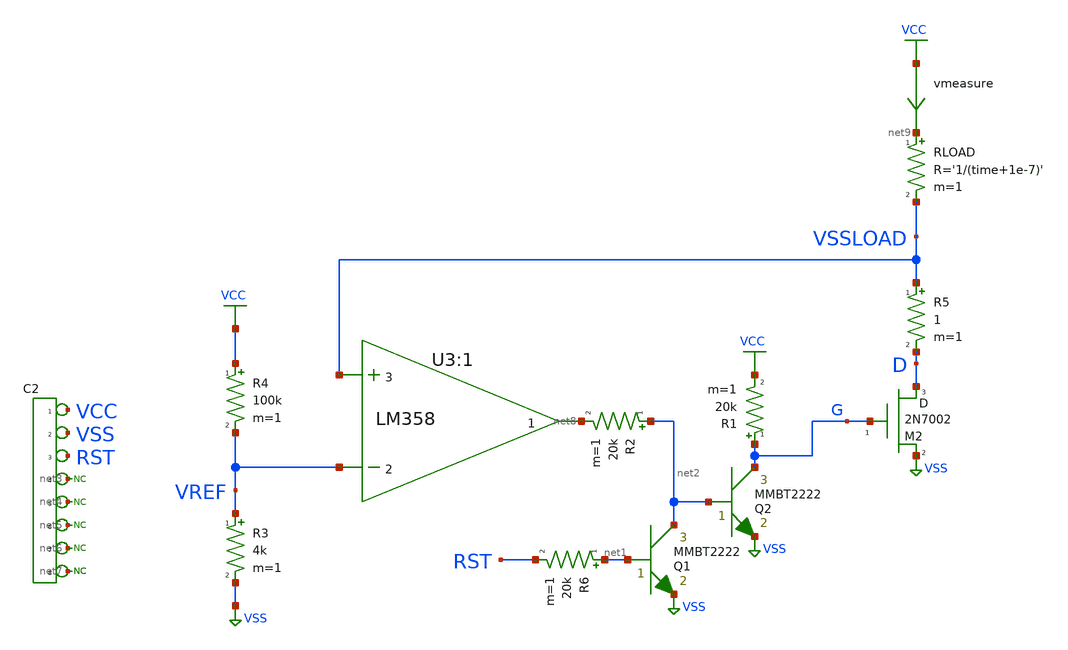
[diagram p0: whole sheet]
** sch_path: xschem_library/pcb/pcb_current_protection.sch
**.subckt pcb_current_protection
*connector(8,1) ?1 VCC ?1 VSS ?1 RST ?1 net3 ?1 net4 ?1 net5 ?1 net6 ?1 net7
* noconn #net7
* noconn #net7
* noconn #net6
XU3:1 VSSLOAD VREF VCC VSS net8 LM358
R3 VREF VSS 4k m=1
R4 VCC VREF 100k m=1
XM2 D G VSS M2N7002 m=1
R5 VSSLOAD D 1 m=1
* noconn #net5
* noconn #net4
* noconn #net3
RLOAD net9 VSSLOAD R='1/(time+1e-7)' m=1
vmeasure VCC net9 0
.save i(vmeasure)
R2 net2 net8 20k m=1
Q1 net2 net1 VSS MMBT2222 area=1 m=1
R6 net1 RST 20k m=1
Q2 G net2 VSS MMBT2222 area=1 m=1
R1 G VCC 20k m=1
**** begin user architecture code


*.option PARHIER=LOCAL RUNLVL=5 post MODMONTE=1 warn maxwarns=400 ingold=1


vvcc vcc 0 dc 5
vvss vss 0 dc 0
vrst rst 0 pwl 0 5 100u 5 101u 0

* .dc RLOAD 10K 1 -0.001
.tran 10u 200m
.save all



.MODEL bd139_2 npn IS=1e-09 BF=222.664 NF=0.85 VAF=36.4079 IKF=0.166126 ISE=5.03418e-09 NE=1.45313
+ BR=1.35467 NR=1.33751 VAR=142.931 IKR=1.66126 ISC=5.02557e-09 NC=3.10227 RB=26.9143 IRB=0.1 RBM=0.1
+ RE=0.000472454 RC=1.04109 XTB=0.727762 XTI=1.04311 EG=1.05 CJE=1e-11 VJE=0.75 MJE=0.33 TF=1e-09 XTF=1 VTF=10
+ ITF=0.01 CJC=1e-11 VJC=0.75 MJC=0.33 XCJC=0.9 FC=0.5 CJS=0 VJS=0.75 MJS=0.5 TR=1e-07 PTF=0 KF=0 AF=1

*SRC=BC817-16;DI_BC817-16;BJTs NPN; Si;  45.0V  0.800A  220MHz   Diodes Inc. BJTs
.MODEL BC817  NPN (IS=4.04n NF=1.00 BF=342 VAF=121  IKF=0.273 ISE=6.86n NE=2.00 BR=4.00 NR=1.00
+  VAR=20.0 IKR=0.675 RE=0.227 RB=0.907 RC=90.7m  XTB=1.5 CJE=107p VJE=1.10 MJE=0.500 CJC=34.7p VJC=0.300
+ MJC=0.300   TF=651p TR=111n EG=1.12 )

.MODEL BD139 NPN ( IS=2.3985E-13 Vceo=80 Icrating=1500m BF=244.9 NF=1.0 BR=78.11 NR=1.007
+ ISE=1.0471E-14 NE=1.2 ISC=1.9314E-11 NC=1.45 VAF=98.5 VAR=7.46 IKF=1.1863 IKR=0.1445 RB=2.14 RBM=0.001 IRB=0.031
+ RE=0.0832 RC=0.01 CJE=2.92702E-10 VJE=0.67412 MJE=0.3300 FC=0.5 CJC=4.8831E-11 VJC=0.5258 MJC=0.3928
+ XCJC=0.5287 XTB=1.1398 EG=1.2105 XTI=3.0)


.MODEL BD140  PNP(IS=1e-09 BF=650.842 NF=0.85 VAF=10 IKF=0.0950125 ISE=1e-08 NE=1.54571 BR=56.177
+ NR=1.5 VAR=2.11267 IKR=0.950125 ISC=1e-08 NC=3.58527 RB=41.7566 IRB=0.1 RBM=0.108893 RE=0.000347052
+ RC=1.32566 XTB=19.5239 XTI=1 EG=1.05 CJE=1e-11 VJE=0.75 MJE=0.33 TF=1e-09 XTF=1 VTF=10 ITF=0.01 CJC=1e-11
+ VJC=0.75 MJC=0.33 XCJC=0.9 FC=0.5 CJS=0 VJS=0.75 MJS=0.5 TR=1e-07 PTF=0 KF=0 AF=10  VCEO=80 ICRATING=1A )


.MODEL Q2N2222A NPN IS =3.0611E-14 NF =1.00124 BF =220 IKF=0.52                VAF=104 ISE=7.5E-15
+ NE =1.41 NR =1.005 BR =4 IKR=0.24                VAR=28 ISC=1.06525E-11 NC =1.3728 RB =0.13 RE =0.22
+                RC =0.12 CJC=9.12E-12 MJC=0.3508 VJC=0.4089                CJE=27.01E-12 TF =0.325E-9 TR =100E-9
+               vce_max=45 vbe_max=6

.MODEL Q2N2222 NPN (  IS = 3.97589E-14 BF = 195.3412 NF = 1.0040078 VAF = 53.081 IKF = 0.976 ISE =
+ 1.60241E-14  NE = 1.4791931 BR = 1.1107942 NR = 0.9928261 VAR = 11.3571702 IKR = 2.4993953 ISC = 1.88505E-12
+  NC = 1.1838278 RB = 56.5826472 IRB = 1.50459E-4 RBM = 5.2592283 RE = 0.0402974 RC = 0.4208  CJE =
+ 2.56E-11 VJE = 0.682256 MJE = 0.3358856 TF = 3.3E-10 XTF = 6 VTF = 0.574  ITF = 0.32 PTF = 25.832 CJC =
+ 1.40625E-11 VJC = 0.5417393 MJC = 0.4547893 XCJC = 1  TR = 3.2E-7 CJS = 0 VJS = .75 MJS = 0 XTB = 1.6486 EG =
+ 1.11  XTI = 5.8315 KF = 0 AF = 1 FC = 0.83               vce_max=45 vbe_max=6 )


* 2n2222 p complementary
.MODEL Q2N2907P PNP(IS=650.6E-18 ISE=54.81E-15 ISC=0 XTI=3  BF=231.7 BR=3.563 IKF=1.079 IKR=0
+ XTB=1.5  VAF=115.7 VAR=35 VJE=0.65 VJC=0.65  RE=0.15 RC=0.715 RB=10  CJE=19.82E-12 CJC=14.76E-12 XCJC=0.75
+ FC=0.5  NF=1 NR=1 NE=1.829 NC=2 MJE=0.3357 MJC=0.5383  TF=603.7E-12 TR=111.3E-9 ITF=0.65 VTF=5 XTF=1.7
+  EG=1.11 KF=1E-9 AF=1  VCEO=45 ICRATING=100M                vce_max=45 vbe_max=6 )

.MODEL Q2N2907S PNP(IS=2.32E-13 ISE=6.69E-16 ISC=1.65E-13 XTI=3.00  BF=3.08E2 BR=2.18E1 IKF=8.42E-1
+ IKR=1.00 XTB=1.5  VAF=1.41E2 VAR=1.35E1 VJE=3.49E-1 VJC=3.00E-1  RE=1.00E-2 RC=8.46E-1 RB=4.02E1 RBM=1.00E-2
+ IRB=1.25E-2  CJE=2.66E-11 CJC=1.93E-11 XCJC=1.00 FC=5.00E-1  NF=1.04 NR=1.12 NE=1.09 NC=1.13 MJE=4.60E-1
+ MJC=4.65E-1  TF=4.95E-10 TR=0 PTF=0 ITF=3.36E-1 VTF=6.54 XTF=1.87E1  EG=1.11 KF=1E-9 AF=1  VCEO=40
+ ICRATING=500M                vce_max=45 vbe_max=6 )





* PINOUT ORDER +IN -IN +V -V OUT
* PINOUT ORDER  1   2   3  4  5
.SUBCKT LM358 1 2 3 4 5
R44 4 6 4E4
I1 4 7 0.5E-6
Q1 4 8 9 QPI
Q2 4 2 10 QPA
Q3 9 9 11 QPI
Q4 10 10 11 QPI
Q5 12 13 4 QNQ
Q6 13 13 4 QNQ
Q7 4 12 14 QPQ
Q8 3 14 6 QNQ
Q9 15 6 4 QNQ
Q10 3 15 16 QNQ
Q11 3 16 17 QNQ
R67 17 16 4E4
R68 5 17 18
Q12 4 15 5 QPQ
Q13 15 17 5 QNQ
I2 18 3 120E-9
I3 19 3 60E-9
I4 20 3 1E-6
Q14 11 18 3 QPQ
Q15 14 19 3 QPQ
Q16 5 7 4 QNQ
Q17 15 20 3 QPQ
C15 21 22 4.8E-12
R69 12 21 3
R70 12 15 3E9
E2 23 8 3 0 -10E-6
V51 23 1 1.56E-3
I6 3 4 5E-6
R71 4 3 4.5E5
Q18 12 9 11 QPQ
Q19 13 10 11 QPQ
C17 12 13 8E-12
C18 6 15 1E-12
C21 3 24 100E-15
R78 11 24 3E5
C22 1 2 0.23E-12
C23 2 0 0.79E-12
C24 1 0 0.79E-12
E3 22 0 15 0 2
C25 5 0 50E-15
Q20 25 25 0 QNQ
G1 3 4 VT 0 3E-4
I7 0 25 1E-3
V53 25 26 0.25
R79 0 26 1E6
E4 VT 0 27 26 1
R80 0 VT 1E6
V54 27 0 0.55
R81 0 27 1E6
.MODEL QPQ PNP IKF=3E-3 RC=300 KF=4.8E-17 BR=1
.MODEL QPA PNP IKF=3E-3 RC=380 IS=1.01E-16 VAF=245 RE=5 RB=1700 BF=300 KF=4.8E-17 BR=1
.MODEL QPI PNP IKF=3E-3 RC=380 IS=1.01E-16 VAF=290 RE=5 RB=1700 BF=306 KF=4.8E-17 BR=1
.MODEL QNQ NPN IKF=5E-3 RC=25  KF=4.8E-17 BR=1
.ENDS
* END SPICE MODEL LM358

.SUBCKT irlml6402 1 2 3
* Node 1 -> Drain
* Node 2 -> Gate
* Node 3 -> Source
M1 9 7 8 8 MM L=100u W=100u
.MODEL MM PMOS LEVEL=1 IS=1e-32 VTO=-1 LAMBDA=0.0111358 KP=12.788 CGSO=5.36099e-06 CGDO=5.54234e-08
RS 8 3 0.0246704
D1 1 3 MD
.MODEL MD D IS=2.03395e-08 RS=0.0432758 N=1.5 BV=20 IBV=0.00025 EG=1 XTI=4 TT=1e-07 CJO=1.11974e-10
+ VJ=0.5 M=0.3 FC=0.5
RDS 3 1 5e+07
RD 9 1 0.0001
RG 2 7 29.2227
D2 5 4 MD1
* Default values used in MD1:
*   RS=0 EG=1.11 XTI=3.0 TT=0
*   BV=infinite IBV=1mA
.MODEL MD1 D IS=1e-32 N=50 CJO=1.68841e-10 VJ=1.50027 M=0.3 FC=1e-08
D3 5 0 MD2
* Default values used in MD2:
*   EG=1.11 XTI=3.0 TT=0 CJO=0
*   BV=infinite IBV=1mA
.MODEL MD2 D IS=1e-10 N=0.4 RS=3e-06
RL 5 10 1
FI2 7 9 VFI2 -1
VFI2 4 0 0
EV16 10 0 9 7 1
CAP 11 10 9.68769e-10
FI1 7 9 VFI1 -1
VFI1 11 6 0
RCAP 6 10 1
D4 6 0 MD3
* Default values used in MD3:
*   EG=1.11 XTI=3.0 TT=0 CJO=0
*   RS=0 BV=infinite IBV=1mA
.MODEL MD3 D IS=1e-10 N=0.4
.ENDS irlml6402

.SUBCKT irf5305s 1 2 3
* Node 1 -> Drain
* Node 2 -> Gate
* Node 3 -> Source
M1 9 7 8 8 MM L=100u W=100u
* Default values used in MM:
* The voltage-dependent capacitances are
* not included. Other default values are:
*   RS=0 RD=0 LD=0 CBD=0 CBS=0 CGBO=0
.MODEL MM PMOS LEVEL=1 IS=1e-32 VTO=-3.45761 LAMBDA=0 KP=10.066 CGSO=1.03141e-05 CGDO=1e-11
RS 8 3 0.0262305
D1 1 3 MD
.MODEL MD D IS=8.90854e-09 RS=0.00921723 N=1.5 BV=55 IBV=0.00025 EG=1.2 XTI=3.13635 TT=1e-07
+ CJO=1.30546e-09 VJ=0.663932 M=0.419045 FC=0.5
RDS 3 1 2.2e+06
RD 9 1 0.0001
RG 2 7 11.0979
D2 5 4 MD1
* Default values used in MD1:
*   RS=0 EG=1.11 XTI=3.0 TT=0
*   BV=infinite IBV=1mA
.MODEL MD1 D IS=1e-32 N=50 CJO=1.63729e-09 VJ=0.791199 M=0.552278 FC=1e-08
D3 5 0 MD2
* Default values used in MD2:
*   EG=1.11 XTI=3.0 TT=0 CJO=0
*   BV=infinite IBV=1mA
.MODEL MD2 D IS=1e-10 N=0.400245 RS=3e-06
RL 5 10 1
FI2 7 9 VFI2 -1
VFI2 4 0 0
EV16 10 0 9 7 1
CAP 11 10 1.89722e-09
FI1 7 9 VFI1 -1
VFI1 11 6 0
RCAP 6 10 1
D4 6 0 MD3
* Default values used in MD3:
*   EG=1.11 XTI=3.0 TT=0 CJO=0
*   RS=0 BV=infinite IBV=1mA
.MODEL MD3 D IS=1e-10 N=0.400245
.ENDS






*MM3725 MCE 5/13/95
*Si    1W  40V 500mA 307MHz pkg:TO-39 3,2,1
.MODEL QMM3725 NPN (IS=50.7F NF=1 BF=162 VAF=113 IKF=.45 ISE=38.2P NE=2  BR=4 NR=1 VAR=24 IKR=.675
+ RE=.263 RB=1.05 RC=.105 XTB=1.5  CJE=62.2P VJE=1.1 MJE=.5 CJC=14.6P VJC=.3 MJC=.3 TF=518P TR=45.9N)

*MPS651 MCE 5/12/95
*Si 625mW  60V    2A 110MHz pkg:TO-92 1,2,3
.MODEL QMPS651 NPN (IS=72.1F NF=1 BF=260 VAF=139 IKF=2.5 ISE=67.1P NE=2  BR=4 NR=1 VAR=20 IKR=3.75
+ RE=28.2M RB=.113 RC=11.3M XTB=1.5  CJE=212P VJE=1.1 MJE=.5 CJC=68.6P VJC=.3 MJC=.3 TF=1.44N TR=1U)

*FCX649 ZETEX Spice model   Last revision  17/7/90   Medium Power
*ZTX Si  1.5W  25V    2A 240MHz pkg:SOT-89 2,1,3
.MODEL QFCX649 NPN(IS=3E-13 BF=225 VAF=80 IKF=2.8 ISE=1.1E-13 NE=1.37   BR=110 NR=0.972 VAR=28
+ IKR=0.8 ISC=6.5E-13 NC=1.372 RB=0.3 RE=0.063   RC=0.07 CJE=3.25E-10 TF=1E-9 CJC=7E-11 TR=1E-8 )

*MPSW01A MCE 5/12/95
*Si    1W  40V    1A 210MHz pkg:TO-92 1,2,3
.MODEL QMPSW01A NPN (IS=18.1F NF=1 BF=273 VAF=113 IKF=.6 ISE=15.7P NE=2  BR=4 NR=1 VAR=20 IKR=.9
+ RE=96.5M RB=.386 RC=38.6M XTB=1.5  CJE=78.7P VJE=1.1 MJE=.5 CJC=17.3P VJC=.3 MJC=.3 TF=757P TR=526N)

*BC546 ZETEX Spice model     Last revision  4/90   General Purpose
*ZTX Si 500mW  65V 200mA 300MHz pkg:TO-92 1,2,3
.MODEL BC546 NPN(IS=1.8E-14 BF=400 NF=0.9955 VAF=80 IKF=0.14 ISE=5E-14   NE=1.46 BR=35.5 NR=1.005
+ VAR=12.5 IKR=0.03 ISC=1.72E-13 NC=1.27 RB=0.56   RE=0.6 RC=0.25 CJE=1.3E-11 TF=6.4E-10 CJC=4E-12 VJC=0.54
+ TR=5.072E-8       vce_max=65 vbe_max=6 )

.MODEL BC857 PNP(        AF= 1.00E+00    BF= 1.96E+02    BR= 3.38E+00   CJC= 9.80E-12       CJE=
+ 1.56E-11   CJS= 0.00E+00    EG= 1.11E+00    FC= 8.28E-01       IKF= 8.35E-01   IKR= 1.60E-02   IRB= 1.31E-06
+    IS= 1.32E-14       ISC= 7.71E-14   ISE= 8.44E-13   ITF= 2.14E-01    KF= 0.00E+00       MJC= 3.49E-01
+   MJE= 4.18E-01   MJS= 3.30E-01    NC= 1.19E+00        NE= 1.83E+00    NF= 1.00E+00    NR= 1.00E+00   PTF=
+ 0.00E+00        RB= 1.00E-02   RBM= 1.00E-02    RC= 1.52E+00    RE= 3.00E-02        TF= 6.05E-10    TR=
+ 0.00E+00   VAF= 5.90E+01   VAR= 1.74E+01       VJC= 3.00E-01   VJE= 8.00E-01   VJS= 7.50E-01   VTF= 4.39E+00
+      XCJC= 1.00E+00   XTB= 0.00E+00   XTF= 5.81E+00   XTI= 3.00E+00)

.MODEL BC556 PNP(       IS=2.059E-14      NF=1.003      ISE=2.971E-15      NE=1.316      BF=227.3
+      IKF=0.08719      VAF=37.2      NR=1.007      ISC=1.339E-14      NC=1.15      BR=7.69      IKR=0.07646
+      VAR=11.42      RB=1      IRB=1E-06      RBM=1      RE=0.688      RC=0.6437      XTB=0      EG=1.11      XTI=3
+      CJE=1.4E-11      VJE=0.5912      MJE=0.3572      TF=7.046E-10      XTF=4.217      VTF=5.367      ITF=0.1947
+      PTF=0      CJC=1.113E-11      VJC=0.1      MJC=0.3414      XCJC=0.6288      TR=1E-32      CJS=0
+      VJS=0.75      MJS=0.333      FC=0.7947      vce_max=65 vbe_max=6 )
*

* NXP Semiconductors
*
* Medium power NPN transistor
* IC   = 1 A
* VCEO = 20 V
* hFE  = 85 - 375 @ 2V/500mA
*
*
*
*
* Package pinning does not match Spice model pinning.
* Package: SOT 223
*
* Package Pin 1: Base
* Package Pin 2: Collector
* Package Pin 3: Emitter
* Package Pin 4: Collector
*
* Extraction date (week/year): 13/2008
* Simulator: Spice 3
*
**********************************************************
*#
.SUBCKT BCP68 1 2 3
*
Q1 1 2 3 BCP68
D1 2 1 DIODE
*
*The diode does not reflect a
*physical device but improves
*only modeling in the reverse
*mode of operation.
*
.MODEL BCP68 NPN   IS = 2.312E-013   NF = 0.988   ISE = 8.851E-014   NE = 2.191   BF = 273   IKF =
+ 5.5   VAF = 50   NR = 0.9885   ISC = 6.808E-014   NC = 3   BR = 155.6   IKR = 4   VAR = 17   RB = 15
+   IRB = 2E-006   RBM = 0.65   RE = 0.073   RC = 0.073   XTB = 0   EG = 1.11   XTI = 3   CJE = 2.678E-010
+   VJE = 0.732   MJE = 0.3484   TF = 5.8E-010   XTF = 1.5   VTF = 2.5   ITF = 1   PTF = 0   CJC =
+ 3.406E-011   VJC = 2   MJC = 0.3142   XCJC = 1   TR = 6.5E-009   CJS = 0   VJS = 0.75   MJS = 0.333   FC =
+ 0.95
.MODEL DIODE D   IS = 2.702E-015   N = 1.2   BV = 1000   IBV = 0.001   RS = 0.1   CJO = 0   VJ = 1
+   M = 0.5   FC = 0   TT = 0   EG = 1.11   XTI = 3
.ENDS

.SUBCKT   D1N5765       2   99
*                      |    |
*                      |    |
*                      |    CATHODE
*                      ANODE
I1  99  4   7.0
D1  2   99   DLOW
D2  2   4   DHIGH
R1  4   99  .1   TC=-6.27E-3,-2.33E-7
*
.MODEL DLOW     D       (          IS = 1.0E-15          RS = 100           N = 2.15          TT =
+ 10.0E-09         CJO = 8.285237E-11          VJ = 1.2076937           M = 0.4053107          EG = 1.664
+         XTI = 10.78          KF = 0          AF = 1          FC = 0.4340008          BV = 5.0         IBV =
+ 1E-4  )
.MODEL DHIGH    D       (          IS = 9.0E-15          RS = 0.30           N = 1.2          TT = 0
+         CJO = 0          VJ = 1           M = .5          EG = 0.1         XTI = -3.84          KF = 0
+          AF = 1          FC = .5          BV = 9.9999E+13         IBV = .001  )
.ENDS

.model D1N4007 D(IS=7.02767n RS=0.0341512 N=1.80803 EG=1.05743 XTI=5 BV=1000 IBV=5e-08 CJO=1e-11
+ VJ=0.7 M=0.5 FC=0.5 TT=1e-07 )

.MODEL D1N4148 D   IS = 4.352E-9   N = 1.906   BV = 110   IBV = 0.0001   RS = 0.6458   CJO =
+ 7.048E-13   VJ = 0.869   M = 0.03   FC = 0.5   TT = 3.48E-9

.MODEL D1n5400 d IS=2.61339e-12 RS=0.0110501 N=1.20576 EG=0.6 XTI=3.1271 BV=50 IBV=1e-05 CJO=1e-11
+ VJ=0.7 M=0.5 FC=0.5 TT=1e-09 KF=0 AF=1
* Model generated on October 12, 2003
* Model format: PSpice


*SYM=POWMOSP
.SUBCKT DMP2035U   10 20 30
*     TERMINALS:  D  G  S
M1   1  2  3  3  PMOS L=0.6U W=0.9
RD  10  1  15m
RS  30  3  4m
RG  20  2  9.45
CGS  2  3  1.42n
EGD 12  30  2  1  1
VFB 14  30  0
FFB  2  1  VFB  1
CGD 13 14  598p
R1  13  30  1.00
D1  13 12  DLIM
DDG 14 15  DCGD
R2  12 15  1.00
D2  30  15  DLIM
DSD 10  3  DSUB
.MODEL PMOS PMOS LEVEL=3 U0=300 VMAX=40k  ETA=0.1m VTO=-1.02 TOX=16.8n NSUB=2e17
.MODEL DCGD D CJO=598p VJ=0.150 M=0.340
.MODEL DSUB D IS=36.1n N=1.50 RS=21.8m BV=20  CJO=40p VJ=0.500 M=0.450
.MODEL DLIM D IS=100U
.ENDS


*March 14, 2005
*Doc. ID: 77621, S-50395, Rev. A
.SUBCKT Si2306BDS 4 1 2
M1  3 1 2 2 NMOS W=573319u L=0.50u
M2  2 1 2 4 PMOS W=573319u L=0.35u
R1  4 3     RTEMP 15E-3
CGS 1 2     110E-12
DBD 2 4     DBD
****************************************************************
.MODEL  NMOS        NMOS ( LEVEL  = 3           TOX    = 5E-8  RS     = 19.5E-3         RD     = 0
+           NSUB   = 1.7E17     kp     = 3.3E-5          UO     = 650               VMAX   = 0               XJ
+     = 5E-7        KAPPA  = 5E-1  ETA    = 1E-4            TPG    = 1    IS     = 0               LD     =
+ 0                               CGSO   = 0               CGDO   = 0           CGBO   = 0   TLEV   = 1
+               BEX    = -1.5        TCV    = 3.9E-3  NFS    = 0.8E12          DELTA  = 0.1)
****************************************************************
.MODEL  PMOS        PMOS ( LEVEL  = 3           TOX    = 5E-8 NSUB    = 2E16            TPG    = -1)
****************************************************************
.MODEL DBD D (CJO=95E-12 VJ=0.38 M=0.20  FC=0.1 IS=1E-12 TT=9.3E-8 N=1 BV=30.2)
****************************************************************
.MODEL RTEMP R (TC1=7E-3 TC2=5.5E-6)
****************************************************************
.ENDS


* Fairchild model
* 2N7002 ELECTRICAL MODEL (SOT-23 Single N-Ch DMOS)
* -----------------------
.SUBCKT  M2N7002  20  10  30
Rg     10    1    1
M1      2    1    3    3    DMOS    L=1u   W=1u
.MODEL DMOS NMOS (VTO='2.1*(-0.0016*TEMPER+1.04)'  KP=0.35  THETA=0.086 VMAX=2.2E5  LEVEL=3)
Cgs     1    3    60p
Rd     20    4    0.3 TC=0.0075
Dds     3    4    DDS
.MODEL     DDS    D(BV='60*(0.00072*TEMPER+0.982)'   M=0.36  CJO=23p   VJ=0.8)
Dbody   3   20    DBODY
.MODEL   DBODY    D(IS=1.4E-13   N=1   RS=40m   TT=100n)
Ra      4    2    0.4 TC=0.0075
Rs      3    5    10m
Ls      5    30   .5n
M2      1    8    6    6   INTER
E2      8    6    4    1   2
.MODEL   INTER    NMOS(VTO=0  KP=10   LEVEL=1)
Cgdmax  7    4    85p
Rcgd    7    4    10meg
Dgd     6    4    DGD
Rdgd    4    6    10meg
.MODEL     DGD    D(M=0.53   CJO=85p   VJ=0.12)
M3      7    9    1    1   INTER
E3      9    1    4    1   -2
.ENDS M2N7002

*SRC=1N4732A;DI_1N4732A;Diodes;Zener <=10V; 4.70V  1.00W   Diodes Inc.  Zener
*SYM=HZEN
.SUBCKT D1N4732A  1   2
*    Terminals    A   K
D1 1 2 DF
DZ 3 1 DR
VZ 2 3 2.99
.MODEL DF D ( IS=87.7p RS=0.620 N=1.10  CJO=214p VJ=0.750 M=0.330 TT=50.1n )
.MODEL DR D ( IS=17.5f RS=0.333 N=2.28 )
.ENDS

* Technology:        DISCRETE DEVICE
* Device:            Zener Diode BZX 55C 5V1
* Type:              Typical (nom)
* Model established: 12.11.1996, by S.Reuter, TM1iC63-HN
* Wafer:
* Remarks:           Macro model
* Revision:
* Simulator:         PSPICE
.SUBCKT BZX5V1 a c

 DF a c DFOR
 DR c a DREV
 DB b a DBRE
 EB c b POLY(1) d 0 3.6 1
 IB 0 d 1m
 RB 0 d 1k TC=3m

.MODEL DFOR D
 + IS =   1p  RS =  3.5  N  =  1.4  CJO= 178p
 + VJ = 610m  M  = 335m  FC = 700m  XTI=    3
 + EG =1.186

.MODEL DREV D
 + IS = 100f  N  =   30  XTI=    3  EG =1.186

.MODEL DBRE D
 + IS =  10f  RS =    6  N  =    1  XTI=    0
 + EG =1.186

.ENDS BZX5V1

.model D1N751_2 D(Is=1.004f Rs=.5875 Ikf=0 N=1 Xti=3 Eg=1.11 Cjo=160p M=.5484 Vj=.75 Fc=.5 Isr=1.8n
+ Nr=2 Bv=5.1 Ibv=27.721m Nbv=1.1779 Ibvl=1.1646m Nbvl=21.894 Tbv1=176.47u Vpk=5.1 )



*(+) 1N751     5.1 V  0.5W  CASE DO-35
.model D1N751  D(Is=1.004f Rs=.5875 Ikf=0 N=1 Xti=3 Eg=1.11 Cjo=160p M=.5484 		Vj=.75 Fc=.5 Isr=1.8n
+ Nr=2 Bv=5.1 Ibv=27.721m Nbv=1.1779 		Ibvl=1.1646m Nbvl=21.894 Tbv1=176.47u)
*		Motorola	pid=1N751	case=DO-35
*		89-9-18-gjg
*		Vz = 5.1 @ 20mA, Zz = 175 @ 1mA, Zz = 8.2 @ 5mA, Zz = 2.2 @ 20mA

* 1N5230    4.7 Volt zener diode
.model D1N5230  D(Is=880.5E-18 Rs=.25 Ikf=0 N=1 Xti=3 Eg=1.11 Cjo=175p M=.5516                Vj=.75
+ Fc=.5 Isr=1.859n Nr=2 Bv=4.7 Ibv=20.245m Nbv=1.6989                Ibvl=1.9556m Nbvl=14.976 Tbv1=-21.28u)
*               Motorola        pid=1N5230      case=DO-35
*               89-9-18 gjg
*               Vz = 4.7 @ 20mA, Zz = 300 @ 1mA, Zz = 12.5 @ 5mA, Zz =2.6  @ 20mA

*1N758
*Ref: Motorola
*10V 500mW Si Zener pkg:DIODE0.4 1,2
.MODEL D1N758 D(IS=1E-11 RS=8.483 N=1.27 TT=5E-8 CJO=2.334E-10 VJ=0.75   M=0.33 BV=9.83 IBV=0.01 )

*1N4744
*Ref: Motorola
*15V 1W Si Zener pkg:DIODE0.4 1,2
.MODEL D1N4744 D(IS=5.32E-14 RS=6.47 TT=5.01E-8 CJO=7.83E-11 M=0.33   BV=14.89 IBV=0.017 )

*1N755
*Ref: Motorola
*7.5V 500mW Si Zener pkg:DIODE0.4 1,2
.MODEL D1N755 D(IS=1E-11 RS=3.359 N=1.27 TT=5E-8 CJO=2.959E-10 VJ=0.75   M=0.33 BV=7.433 IBV=0.01 )

** node order
* 1: gnd
* 2: trig
* 3: out
* 4: reset#
* 5: ctrl
* 6: thres
* 7: dis
* 8: vcc
.SUBCKT ne555  34 32 30 19 23 33 1  21
*              G  TR O  R  F  TH D  V
Q4 25 2 3 QP
Q5 34 6 3 QP
Q6 6 6 8 QP
R1 9 21 4.7K
R2 3 21 830
R3 8 21 4.7K
Q7 2 33 5 QN
Q8 2 5 17 QN
Q9 6 4 17 QN
Q10 6 23 4 QN
Q11 12 20 10 QP
R4 10 21 1K
Q12 22 11 12 QP
Q13 14 13 12 QP
Q14 34 32 11 QP
Q15 14 18 13 QP
R5 14 34 100K
R6 22 34 100K
R7 17 34 10K
Q16 1 15 34 QN
Q17 15 19 31 QP
R8 18 23 5K
R9 18 34 5K
R10 21 23 5K
Q18 27 20 21 QP
Q19 20 20 21 QP
R11 20 31 5K
D1 31 24 DA
Q20 24 25 34 QN
Q21 25 22 34 QN
Q22 27 24 34 QN
R12 25 27 4.7K
R13 21 29 6.8K
Q23 21 29 28 QN
Q24 29 27 16 QN
Q25 30 26 34 QN
Q26 21 28 30 QN
D2 30 29 DA
R14 16 15 100
R15 16 26 220
R16 16 34 4.7K
R17 28 30 3.9K
Q3 2 2 9 QP
.MODEL DA D (RS=40 IS=1.0E-14 CJO=1PF)
.MODEL QP PNP (level=1 BF=20 BR=0.02 RC=4 RB=25 IS=1.0E-14 VA=50 NE=2)  CJE=12.4P VJE=1.1 MJE=.5
+ CJC=4.02P VJC=.3 MJC=.3 TF=229P TR=159N)
.MODEL QN NPN (level=1 IS=5.07F NF=1 BF=100 VAF=161 IKF=30M ISE=3.9P NE=2  BR=4 NR=1 VAR=16 IKR=45M
+ RE=1.03 RB=4.12 RC=.412 XTB=1.5  CJE=12.4P VJE=1.1 MJE=.5 CJC=4.02P VJC=.3 MJC=.3 TF=229P TR=959P)
.ENDS

.SUBCKT BS250P 3 4 5
*              D G S
M1 3 2 5 5 MBS250
RG 4 2 160
RL 3 5 1.2E8
C1 2 5 47E-12
C2 3 2 10E-12
D1 3 5 DBS250
*
.MODEL MBS250 PMOS VTO=-3.193 RS=2.041 RD=0.697 IS=1E-15 KP=0.277 CBD=105E-12 PB=1 LAMBDA=1.2E-2
.MODEL DBS250 D IS=2E-13 RS=0.309
.ENDS BS250P

.SUBCKT BS170 3 4 5
*             D G S
M1 3 2 5 5 N3306M
RG 4 2 270
RL 3 5 1.2E8
C1 2 5 28E-12
C2 3 2 3E-12
D1 5 3 N3306D
*
.MODEL N3306M NMOS VTO=1.824 RS=1.572 RD=1.436 IS=1E-15 KP=.1233 CBD=35E-12 PB=1
.MODEL N3306D D IS=5E-12 RS=.768
.ENDS BS170
*

.SUBCKT irf540 1 2 3
* Node 1 -> Drain
* Node 2 -> Gate
* Node 3 -> Source
M1 9 7 8 8 MM L=100u W=100u
* Default values used in MM:
* The voltage-dependent capacitances are
* not included. Other default values are:
* RS=0 RD=0 LD=0 CBD=0 CBS=0 CGBO=0
.MODEL MM NMOS LEVEL=1 IS=1e-32 VTO=3.56362 LAMBDA=0.00291031 KP=25.0081 CGSO=1.60584e-05
+ CGDO=4.25919e-07
RS 8 3 0.0317085
D1 3 1 MD
.MODEL MD D IS=1.02194e-10 RS=0.00968022 N=1.21527 BV=100 IBV=0.00025 EG=1.2 XTI=3.03885 TT=1e-07
+ CJO=1.81859e-09 VJ=1.1279 M=0.449161 FC=0.5
RDS 3 1 4e+06
RD 9 1 0.0135649
RG 2 7 5.11362
D2 4 5 MD1
* Default values used in MD1:
* RS=0 EG=1.11 XTI=3.0 TT=0
* BV=infinite IBV=1mA
.MODEL MD1 D IS=1e-32 N=50 CJO=2.49697e-09 VJ=0.5 M=0.9 FC=1e-08
D3 0 5 MD2
* Default values used in MD2:
* EG=1.11 XTI=3.0 TT=0 CJO=0
* BV=infinite IBV=1mA
.MODEL MD2 D IS=1e-10 N=0.4 RS=3e-06
RL 5 10 1
FI2 7 9 VFI2 -1
VFI2 4 0 0
EV16 10 0 9 7 1
CAP 11 10 2.49697e-09
FI1 7 9 VFI1 -1
VFI1 11 6 0
RCAP 6 10 1
D4 0 6 MD3
* Default values used in MD3:
* EG=1.11 XTI=3.0 TT=0 CJO=0
* RS=0 BV=infinite IBV=1mA
.MODEL MD3 D IS=1e-10 N=0.4
.ENDS




*LM5134A
*****************************************************************************
.SUBCKT LM5134A VDD PILOT OUT IN INB VSS
E_E2         INB_INT 0 INB VSS 1
C_U3_C1         U3_N16789866 U3_N16789873  5p
X_U3_U5         VDD U3_N16789873 U3_N16790218 0 RVAR  RREF=1
C_U3_C3         OUT U3_N16789866  1p

* E_U3_E1         U3_N16790231 OUT vol=' V(MGATE, 0) > 0.5? 5: -5'
E_U3_E1         U3_N16790231 OUT pwl(1) MGATE 0 0.49 -5 0.51 5

X_U3_U6         U3_N24836 VSS U3_N31827 0 RVAR   RREF=1
R_U3_R1         U3_N16790231 U3_N16789866  20
M_U3_M2         U3_N24836 U3_N16789871 OUT OUT PMOS01
E_U3_E4         U3_N16790218 0 pwl(1) VDD_INT 0   0 0, 4.5 0.9, 10  0.09, 12.6 0.08
X_U3_U10         VSS OUT d_d1
R_U3_R2         U3_N16789868 U3_N16789871  20
C_U3_C2         U3_N24836 U3_N16789871  5p
X_U3_U9         OUT VDD d_d1
C_U3_C5         OUT VDD  10p
C_U3_C6         OUT U3_N16789871  10p
C_U3_C4         VSS OUT  10p
M_U3_M1         U3_N16789873 U3_N16789866 OUT OUT NMOS01
E_U3_E3         U3_N31827 0 pwl(1) VDD_INT 0      0 0, 4.5  0.26, 10  0.01, 12.6 0.01
E_U3_E2         OUT U3_N16789868 vol= 'V(MGATE, 0) > 0.5? -5: 5'
E_U4_ABM4         U4_N14683241 0 vol= 'V(U4_ON_INT) >=0.5?V(VDD_INT):0'
C_U4_C3         U4_N14683221 0  1n
V_U4_V6         U4_N155225261 0 80m
R_U4_R2         U4_N14683241 U4_N14683221  1
X_U4_U47         U4_N14683247 U4_N14683251 d_d1
E_U4_ABM5         U4_N14683301 0 vol= 'V(U4_ON_INT)<0.5? V(VDD_INT):0'
C_U4_C1         U4_N14683247 0  1n
X_U4_S1    U4_N14683159 0 U4_N14683247 0 PTON_TOFF_U4_S1
X_U4_U44         U4_ON_INT PGATE U4_N14683147 AND2_BASIC_GEN  VDD=1   VSS=0 VTHRESH=500E-3
X_U4_U43         U4_N14683247 PGATE BUF_BASIC_GEN VDD=1 VSS=0   VTHRESH=0.5
R_U4_R3         U4_N14683301 U4_N14683281  1
X_U4_U7         N18232068 U4_N15541612 INV_BASIC_GEN  VDD=1 VSS=0   VTHRESH=500E-3
G_U4_G1         U4_N14683251 U4_N14683247 pwl(1) U4_N14683221 0      0 0, 4.5 140m, 10 500m, 12.6
+ 600m
G_U4_G2         U4_N14683247 0 pwl(1) U4_N14683281 0      0 0, 4.5 70m, 10 800m, 12.6 900m
X_U4_U8         MGATE U4_N15541600 INV_BASIC_GEN  VDD=1 VSS=0   VTHRESH=500E-3
C_U4_C4         U4_N14683281 0  1n
X_U4_S2    U4_N14683147 0 U4_N14683251 U4_N14683247 PTON_TOFF_U4_S2
X_U4_U48         U4_N155225261 U4_N14683247 d_d1
X_U4_U45         U4_N15541600 U4_N15541612 U4_ON_INT AND2_BASIC_GEN    VDD=1 VSS=0 VTHRESH=500E-3
V_U4_V5         U4_N14683251 0 1V
X_U4_U46         PGATE U4_ON_INT U4_N14683159 NOR2_BASIC_GEN  VDD=1   VSS=0 VTHRESH=500E-3
E_E1         IN_INT 0 IN VSS 1
E_E3         VDD_INT 0 VDD VSS 1
C_U2_C1         U2_N14683247 0  1n
X_U2_U46         MGATE U2_ON_INT U2_N14683159 NOR2_BASIC_GEN  VDD=1   VSS=0 VTHRESH=500E-3
X_U2_U7         PGATE U2_N15532894 INV_BASIC_GEN  VDD=1 VSS=0   VTHRESH=500E-3
G_U2_G1         U2_N14683251 U2_N14683247 pwl(1)  U2_N14683221 0      0 0,  4.5 58m,  10 140m,  12.6
+ 230m

E_U2_ABM5         U2_N14683301 0 vol= 'V(U2_ON_INT) <0.5? V(VDD_INT):0'

X_U2_U43         U2_N14683247 MGATE BUF_BASIC_GEN VDD=1 VSS=0   VTHRESH=0.5
X_U2_U48         U2_N147032561 U2_N14683247 d_d1
V_U2_V6         U2_N147032561 0 80m
X_U2_S2    U2_N14683147 0 U2_N14683251 U2_N14683247 MTON_TOFF_U2_S2

E_U2_ABM4         U2_N14683241 0 vol='V(U2_ON_INT) >=0.5? V(VDD_INT):0  '

R_U2_R2         U2_N14683241 U2_N14683221  1
G_U2_G2         U2_N14683247 0 PWL(1) U2_N14683281 0      0 0, 4.5 32m, 10 90m, 12.6 160m
V_U2_V5         U2_N14683251 0 1V
X_U2_U44         U2_ON_INT MGATE U2_N14683147 AND2_BASIC_GEN  VDD=1   VSS=0 VTHRESH=500E-3
C_U2_C3         U2_N14683221 0  1n
X_U2_U45         N18232068 U2_N15532894 U2_ON_INT AND2_BASIC_GEN  VDD=1   VSS=0 VTHRESH=500E-3
X_U2_S1    U2_N14683159 0 U2_N14683247 0 MTON_TOFF_U2_S1
R_U2_R3         U2_N14683301 U2_N14683281  1
C_U2_C4         U2_N14683281 0  1n
X_U2_U47         U2_N14683247 U2_N14683251 d_d1
X_U1_U6         INB_INT U1_VIH U1_VHYS U1_N15517298 COMPHYS_BASIC_GEN    VDD=1 VSS=0 VTHRESH=0.5
R_U1_R1         U1_N15521766 U1_VDD_UVLO  721.5
X_U1_U7         U1_N15517298 U1_INB_OUT INV_BASIC_GEN  VDD=1 VSS=0   VTHRESH=500E-3
X_U1_U9         U1_IN_OUT U1_INB_OUT U1_VDD_UVLO N18232068 AND3_BASIC_GEN    VDD=1 VSS=0
+ VTHRESH=500E-3
C_U1_C1         U1_VDD_UVLO 0  1n
X_U1_U5         IN_INT U1_VIH U1_VHYS U1_IN_OUT COMPHYS_BASIC_GEN  VDD=1   VSS=0 VTHRESH=0.5
X_U1_U8         VDD_INT U1_N15521824 U1_N15521760 U1_N15521766   COMPHYS_BASIC_GEN  VDD=1 VSS=0
+ VTHRESH=0.5
V_U1_V1         U1_N15521824 0 3.6
E_U1_ABM3         U1_VHYS 0 vol= '0.34*V(VDD_INT)'
E_U1_ABM1         U1_VIH 0 vol='0.67*V(VDD_INT)'
V_U1_V2         U1_N15521760 0 0.36
X_U1_U35         U1_VDD_UVLO U1_N15521766 d_d1
M_U5_M2         U5_N16789896 U5_N23038 PILOT PILOT PMOS02
R_U5_R1         U5_N16790231 U5_N16789866  20
X_U5_U6         U5_N16789896 VSS U5_N16802670 0 RVAR  RREF=1
M_U5_M1         U5_N08221 U5_N16789866 PILOT PILOT NMOS02
C_U5_C4         VSS PILOT  10p
C_U5_C2         U5_N16789896 U5_N23038  5p
R_U5_R2         U5_N16789868 U5_N23038  20
E_U5_E3         U5_N16802670 0 pwl(1) VDD_INT 0      0 0, 4.5 2.8, 10 1.9, 12.6 1.6
X_U5_U5         VDD U5_N08221 U5_N26349 0 RVAR RREF=1
C_U5_C1         U5_N08221 U5_N16789866  5p
C_U5_C5         PILOT VDD  10p
E_U5_E4         U5_N26349 0 pwl(1) VDD_INT 0      0 0, 4.5 9.5, 10 2.88, 12.6 2.8
X_U5_U9         PILOT VDD d_d1
C_U5_C3         PILOT U5_N16789866  10p
X_U5_U10         VSS PILOT d_d1
E_U5_E2         PILOT U5_N16789868 vol= ' V(PGATE, 0) > 0.5? -5: 5'
E_U5_E1         U5_N16790231 PILOT vol= ' V(PGATE, 0) > 0.5? 5: -5'
C_U5_C6         PILOT U5_N23038  10p
.ENDS LM5134A
*$
.SUBCKT PTON_TOFF_U4_S1 1 2 3 4
G_Switch 3 4 VCR PWL(1) 1 2 0.2 100e6 0.8 1m
RS_U4_S1         1 2 1G
.ENDS PTON_TOFF_U4_S1
*$
.SUBCKT PTON_TOFF_U4_S2 1 2 3 4
G_Switch 3 4 VCR PWL(1) 1 2 0.2 100e6 0.8 1m
RS_U4_S2         1 2 1G
.ENDS PTON_TOFF_U4_S2
*$
.SUBCKT MTON_TOFF_U2_S2 1 2 3 4
G_Switch 3 4 VCR PWL(1) 1 2 0.2 100e6 0.8 1m
RS_U2_S2         1 2 1G
.ENDS MTON_TOFF_U2_S2
*$
.SUBCKT MTON_TOFF_U2_S1 1 2 3 4
G_Switch 3 4 VCR PWL(1) 1 2 0.2 100e6 0.8 1m
RS_U2_S1         1 2 1G
.ENDS MTON_TOFF_U2_S1
*$
****************************** Basic Components **************************
.SUBCKT D_D1 1 2
D1 1 2 DD1
.MODEL DD1 D (IS=1e-15 Rs=0.001 N=0.1  TT=10p)
.ENDS D_D1
*$
.SUBCKT BUF_BASIC_GEN A  Y VDD=1 VSS=0 VTHRESH=0.5
* E_ABMGATE    YINT 0 vol='V(A) > VTHRESH? VDD:VSS'
E_ABMGATE    YINT 0 pwl(1) A 0 'VTHRESH-0.01' VSS 'VTHRESH+0.01' VDD
RINT YINT Y 1
CINT Y 0 1n
.ENDS BUF_BASIC_GEN
*$
.MODEL NMOS01 NMOS (VTO = 2 KP = 1.005 LAMBDA  = 0.001)
*$
.MODEL PMOS01 PMOS (VTO = -2 KP = 1.77 LAMBDA  = 0.001)
*$
.MODEL NMOS02 NMOS (VTO = 2 KP = 0.1814 LAMBDA = 0.001)
*$
.MODEL PMOS02 PMOS (VTO = -2 KP = 0.2497 LAMBDA = 0.001)
*$
.SUBCKT COMPHYS_BASIC_GEN INP INM HYS OUT VDD=1 VSS=0 VTHRESH=0.5
EIN INP1 INM1 INP INM 1
* EHYS INP1 INP2 vol='V(1) > VTHRESH? -V(HYS):0'
EHYS INP1 INP2 pwl(1) 1 0 'VTHRESH-0.01' 0 'VTHRESH+0.01' '-V(HYS)'

EOUT OUT 0 vol='V(INP2)>V(INM1)? VDD : VSS'
R1 OUT 1 1
C1 1 0 5n
RINP1 INP1 0 1K
.ENDS COMPHYS_BASIC_GEN
*$
.SUBCKT AND2_BASIC_GEN A B Y  VDD=1 VSS=0 VTHRESH=0.5
E_ABMGATE    YINT 0 vol= 'V(A) > VTHRESH  && V(B) > VTHRESH ? VDD:VSS'
RINT YINT Y 1
CINT Y 0 1n
.ENDS AND2_BASIC_GEN
*$
.SUBCKT NOR2_BASIC_GEN A B Y  VDD=1 VSS=0 VTHRESH=0.5
E_ABMGATE    YINT 0 vol= 'V(A) > VTHRESH  || V(B) > VTHRESH ? VSS:VDD'
RINT YINT Y 1
CINT Y 0 1n
.ENDS NOR2_BASIC_GEN
*$
.SUBCKT AND3_BASIC_GEN A B C Y VDD=1 VSS=0 VTHRESH=0.5
E_ABMGATE    YINT 0 vol= 'V(A) > VTHRESH  &&  V(B) > VTHRESH && V(C) > VTHRESH ? VDD:VSS'
RINT YINT Y 1
CINT Y 0 1n
.ENDS AND3_BASIC_GEN
*$
.SUBCKT INV_BASIC_GEN A  Y VDD=1 VSS=0 VTHRESH=0.5
* E_ABMGATE    YINT 0 vol='V(A) > VTHRESH ? VSS : VDD'
E_ABMGATE    YINT 0 pwl(1) A 0 'VTHRESH-0.01' VDD 'VTHRESH+0.01' VSS
RINT YINT Y 1
CINT Y 0 1n
.ENDS INV_BASIC_GEN
*$
.SUBCKT RVAR 101 102 201 202 RREF=1
* nodes : 101 102 : nodes between which variable resistance is placed
* 201 202 : nodes to whose voltage the resistance is proportional
* parameters : rref : reference value of the resistance
rin 201 202 1G   $$ input resistance
r 301 0 rref
fcopy 0 301 vsense 1 $$  copy output current thru Z
eout 101 106 poly(2) 201 202 301 0 0 0 0 0 1   $$ multiply VoverZ with Vctrl
vsense 106 102 0   $$ sense iout
.ENDS RVAR
*$


* (REV N/A)    SUPPLY VOLTAGE: 5V
* CONNECTIONS: NON-INVERTING INPUT
*              | INVERTING INPUT
*              | | POSITIVE POWER SUPPLY
*              | | | NEGATIVE POWER SUPPLY
*              | | | | OUTPUT
*              | | | | |
.SUBCKT LM324  1 2 3 4 5
*
  C1   11 12 5.544E-12
  C2    6  7 20.00E-12
  DC    5 53 DX
  DE   54  5 DX
  DLP  90 91 DX
  DLN  92 90 DX
  DP    4  3 DX
  EGND 99  0 POLY(2) (3,0) (4,0) 0 .5 .5
  FB    7 99 POLY(5) VB VC VE VLP VLN 0 15.91E6 -20E6 20E6 20E6 -20E6
  GA    6  0 11 12 125.7E-6
  GCM   0  6 10 99 7.067E-9
  IEE   3 10 DC 10.04E-6
  HLIM 90  0 VLIM 1K
  Q1   11  2 13 QX
  Q2   12  1 14 QX
  R2    6  9 100.0E3
  RC1   4 11 7.957E3
  RC2   4 12 7.957E3
  RE1  13 10 2.773E3
  RE2  14 10 2.773E3
  REE  10 99 19.92E6
  RO1   8  5 50
  RO2   7 99 50
  RP    3  4 30.31E3
  VB    9  0 DC 0
  VC 3 53 DC 2.100
  VE   54  4 DC .6
  VLIM  7  8 DC 0
  VLP  91  0 DC 40
  VLN   0 92 DC 40
.MODEL DX D(IS=800.0E-18)
.MODEL QX PNP(IS=800.0E-18 BF=250)
.ENDS


*LM317 TI voltage regulator - pin order: In, Adj, Out
*TI adjustable voltage regulator pkg:TO-3
.SUBCKT LM317 1 2 3 **Changes my be required on this line**
J1 1 3 4 JN
Q2 5 5 6 QPL .1
Q3 5 8 9 QNL .2
Q4 8 5 7 QPL .1
Q5 81 8 3 QNL .2
Q6 3 81 10 QPL .2
Q7 12 81 13 QNL .2
Q8 10 5 11 QPL .2
Q9 14 12 10 QPL .2
Q10 16 5 17 QPL .2
Q11 16 14 15 QNL .2
Q12 3 20 16 QPL .2
Q13 1 19 20 QNL .2
Q14 19 5 18 QPL .2
Q15 3 21 19 QPL .2
Q16 21 22 16 QPL .2
Q17 21 3 24 QNL .2
Q18 22 22 16 QPL .2
Q19 22 3 241 QNL 2
Q20 3 25 16 QPL .2
Q21 25 26 3 QNL .2
Q22A 35 35 1 QPL 2
Q22B 16 35 1 QPL 2
Q23 35 16 30 QNL 2
Q24A 27 40 29 QNL .2
Q24B 27 40 28 QNL .2
Q25 1 31 41 QNL 5
Q26 1 41 32 QNL 50
D1 3 4 DZ
D2 33 1 DZ
D3 29 34 DZ
R1 1 6 310
R2 1 7 310
R3 1 11 190
R4 1 17 82
R5 1 18 5.6K
R6 4 8 100K
R7 8 81 130
R8 10 12 12.4K
R9 9 3 180
R10 13 3 4.1K
R11 14 3 5.8K
R12 15 3 72
R13 20 3 5.1K
R14 2 24 12K
R15 24 241 2.4K
R16 16 25 6.7K
R17 16 40 12K
R18 30 41 130
R19 16 31 370
R20 26 27 13K
R21 27 40 400
R22 3 41 160
R23 33 34 18K
R24 28 29 160
R25 28 32 3
R26 32 3 .1
C1 21 3 30PF
C2 21 2 30PF
C3 25 26 5PF
CBS1 5 3 2PF
CBS2 35 3 1PF
CBS3 22 3 1PF
.MODEL JN NJF(BETA=1E-4 VTO=-7)
.MODEL DZ D(BV=6.3)
.MODEL QNL NPN(EG=1.22 BF=80 RB=100 CCS=1.5PF TF=.3NS TR=6NS CJE=2PF  CJC=1PF VAF=100)
.MODEL QPL PNP(BF=40 RB=20 TF=.6NS TR=10NS CJE=1.5PF CJC=1PF VAF=50)
.ENDS

.SUBCKT xxxxLM317 1 3 2
* IN ADJ OUT
IADJ 1 4 50U
VREF 4 3 1.25
RC 1 14 0.742
DBK 14 13 D1
CBC 13 15 2.479N
RBC 15 5 247
QP 13 5 2 Q1
RB2 6 5 124
DSC 6 11 D1
ESC 11 2 POLY(2) (13,5) (6,5) 2.85  0 0 0 -70.1M
DFB 6 12 D1
EFB 12 2 POLY(2) (13,5) (6,5) 3.92  -135M 0 1.21M -70.1M
RB1 7 6 1
EB 7 2 8 2 2.56
CPZ 10 2 0.796U
DPU 10 2 D1
RZ 8 10 0.104
RP 9 8 100
EP 9 2 4 2 103.6
RI 2 4 100MEG
.MODEL Q1 NPN (IS=30F BF=100  VAF=14.27 NF=1.604)
.MODEL D1 D (IS=30F N=1.604)
.ENDS



.SUBCKT LM337 8 1 19
*Connections Input Adj. Output
*LM337 negative voltage regulator
.MODEL QN NPN (BF=50 TF=1N CJC=1P)
.MODEL QPOUT PNP (BF=50 TF=1N RE=.2 CJC=1P)
.MODEL QP PNP CJC=1P TF=2N
.MODEL DN D
.MODEL D2 D BV=12 IBV=100U
R10 25 6 1K
Q3 8 17 16 QPOUT
Q4 8 25 17 QP
R18 19 17 250
R19 19 16 .3
G1 8 6 1 18 .1
C7 6 2 .04U
R24 2 8 100
I_ADJ 0 1 65U
R26 8 25 200K
Q5 25 4 19 QP
R27 16 4 200
R28 7 4 7K
D1 8 7 D2
D2 8 6 DN
V1 18 19 1.25
.ENDS


**** end user architecture code
**.ends
.GLOBAL VSS
.GLOBAL VCC
.end
